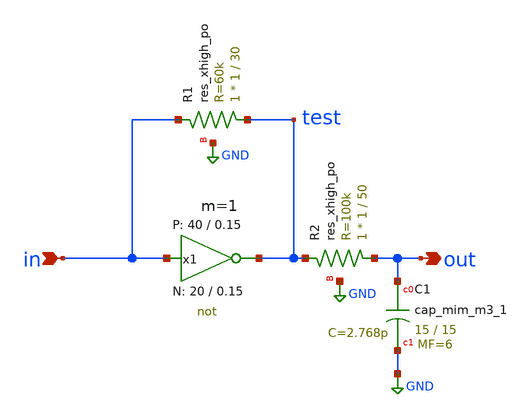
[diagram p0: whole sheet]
** sch_path: Amplifier_Inv/xschem/inv_sky130_a_v0.sch
* StefanSchippers/xschem_sky130/sky130_tests/not.sch:
* Copyright 2021 Stefan Frederik Schippers
* Licensed under the Apache License, Version 2.0 (the "License");
**.subckt inv_sky130_a_v0 in out
*.ipin in
*.opin out
x1 test in VCC VSS not W_N=20 L_N=0.15 W_P=40 L_P=0.15 m=1
XC1 out GND sky130_fd_pr__cap_mim_m3_1 W=15 L=15 MF=6 m=6
XR1 test in GND sky130_fd_pr__res_xhigh_po W=1 L=30 mult=1 m=1
XR2 out test GND sky130_fd_pr__res_xhigh_po W=1 L=50 mult=1 m=1
**.ends

* expanding   symbol:  sky130_tests/not.sym # of pins=2
** sym_path: sky130_tests/not.sym
** sch_path: sky130_tests/not.sch
.subckt not y a VCCPIN VSSPIN     W_N=1 L_N=0.15 W_P=2 L_P=0.15
*.opin y
*.ipin a
XM1 DN a VSSPIN VSSPIN sky130_fd_pr__nfet_01v8 L=L_N W=W_N nf=1 ad='int((1 + 1)/2) * W_N / 1 * 0.29'
+ as='int((1 + 2)/2) * W_N / 1 * 0.29' pd='2*int((1 + 1)/2) * (W_N / 1 + 0.29)' ps='2*int((1 + 2)/2) * (W_N / 1 + 0.29)'
+ nrd='0.29 / W_N ' nrs='0.29 / W_N ' sa=0 sb=0 sd=0 mult=1 m=1
XM2 DP a VCCPIN VCCPIN sky130_fd_pr__pfet_01v8 L=L_P W=W_P nf=1 ad='int((nf+1)/2) * W/nf * 0.29' as='int((nf+2)/2) * W/nf * 0.29'
+ pd='2*int((nf+1)/2) * (W/nf + 0.29)' ps='2*int((nf+2)/2) * (W/nf + 0.29)' nrd='0.29 / W' nrs='0.29 / W'
+ sa=0 sb=0 sd=0 mult=1 m=1
Vmeas DP y 0
.save i(vmeas)
Vmeas1 y DN 0
.save i(vmeas1)
.save v(dp)
.save v(dn)
.ends

.GLOBAL GND
.end
